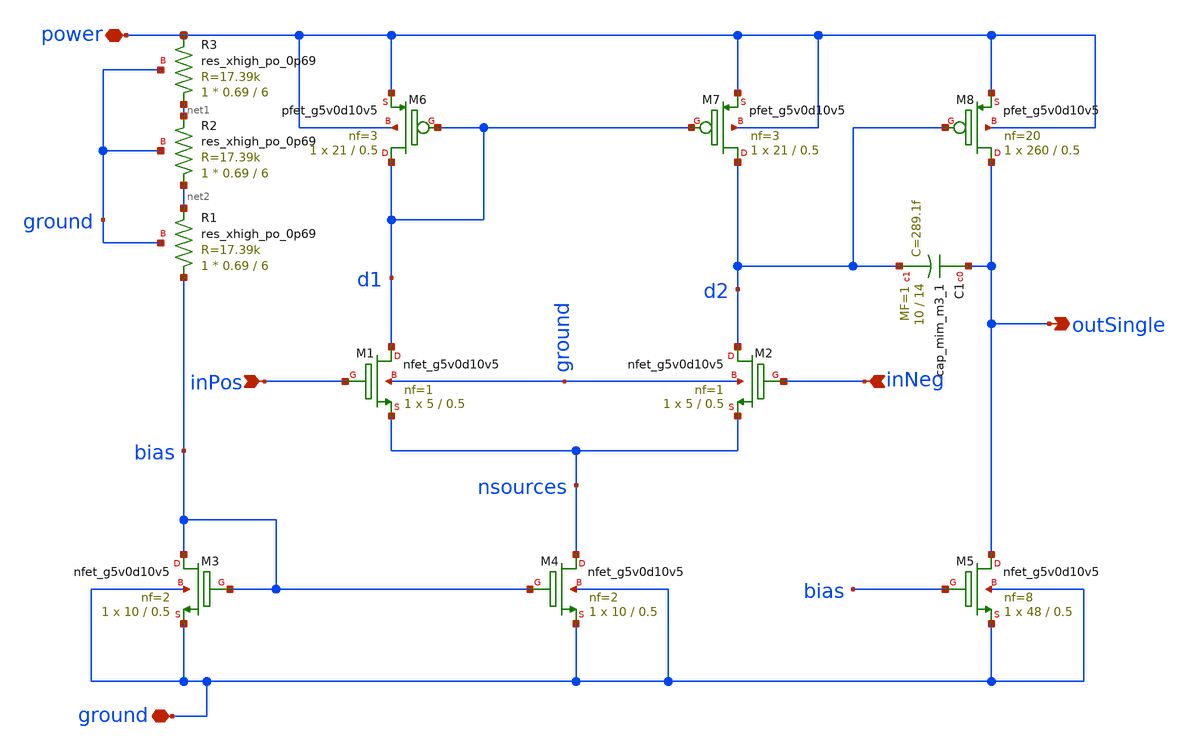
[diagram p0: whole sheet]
** sch_path: dev/opamp/miel21_opamp.sch
**.subckt miel21_opamp inPos inNeg outSingle power ground
*.ipin inPos
*.ipin inNeg
*.opin outSingle
*.iopin power
*.iopin ground
XM6 d1 d1 power power sky130_fd_pr__pfet_g5v0d10v5 L=0.5 W=21 nf=3 ad='int((nf+1)/2) * W/nf * 0.29' as='int((nf+2)/2) * W/nf * 0.29'
+ pd='2*int((nf+1)/2) * (W/nf + 0.29)' ps='2*int((nf+2)/2) * (W/nf + 0.29)' nrd='0.29 / W' nrs='0.29 / W'
+ sa=0 sb=0 sd=0 mult=1 m=1
XM7 d2 d1 power power sky130_fd_pr__pfet_g5v0d10v5 L=0.5 W=21 nf=3 ad='int((nf+1)/2) * W/nf * 0.29' as='int((nf+2)/2) * W/nf * 0.29'
+ pd='2*int((nf+1)/2) * (W/nf + 0.29)' ps='2*int((nf+2)/2) * (W/nf + 0.29)' nrd='0.29 / W' nrs='0.29 / W'
+ sa=0 sb=0 sd=0 mult=1 m=1
XM8 outSingle d2 power power sky130_fd_pr__pfet_g5v0d10v5 L=0.5 W=260 nf=20 ad='int((nf+1)/2) * W/nf * 0.29'
+ as='int((nf+2)/2) * W/nf * 0.29' pd='2*int((nf+1)/2) * (W/nf + 0.29)' ps='2*int((nf+2)/2) * (W/nf + 0.29)'
+ nrd='0.29 / W' nrs='0.29 / W' sa=0 sb=0 sd=0 mult=1 m=1
XM1 d1 inPos nsources ground sky130_fd_pr__nfet_g5v0d10v5 L=0.5 W=5 nf=1 ad='int((nf+1)/2) * W/nf * 0.29'
+ as='int((nf+2)/2) * W/nf * 0.29' pd='2*int((nf+1)/2) * (W/nf + 0.29)' ps='2*int((nf+2)/2) * (W/nf + 0.29)'
+ nrd='0.29 / W' nrs='0.29 / W' sa=0 sb=0 sd=0 mult=1 m=1
XM2 d2 inNeg nsources ground sky130_fd_pr__nfet_g5v0d10v5 L=0.5 W=5 nf=1 ad='int((nf+1)/2) * W/nf * 0.29'
+ as='int((nf+2)/2) * W/nf * 0.29' pd='2*int((nf+1)/2) * (W/nf + 0.29)' ps='2*int((nf+2)/2) * (W/nf + 0.29)'
+ nrd='0.29 / W' nrs='0.29 / W' sa=0 sb=0 sd=0 mult=1 m=1
XM3 bias bias ground ground sky130_fd_pr__nfet_g5v0d10v5 L=0.5 W=10 nf=2 ad='int((nf+1)/2) * W/nf * 0.29'
+ as='int((nf+2)/2) * W/nf * 0.29' pd='2*int((nf+1)/2) * (W/nf + 0.29)' ps='2*int((nf+2)/2) * (W/nf + 0.29)'
+ nrd='0.29 / W' nrs='0.29 / W' sa=0 sb=0 sd=0 mult=1 m=1
XM4 nsources bias ground ground sky130_fd_pr__nfet_g5v0d10v5 L=0.5 W=10 nf=2 ad='int((nf+1)/2) * W/nf * 0.29'
+ as='int((nf+2)/2) * W/nf * 0.29' pd='2*int((nf+1)/2) * (W/nf + 0.29)' ps='2*int((nf+2)/2) * (W/nf + 0.29)'
+ nrd='0.29 / W' nrs='0.29 / W' sa=0 sb=0 sd=0 mult=1 m=1
XM5 outSingle bias ground ground sky130_fd_pr__nfet_g5v0d10v5 L=0.5 W=48 nf=8 ad='int((nf+1)/2) * W/nf * 0.29'
+ as='int((nf+2)/2) * W/nf * 0.29' pd='2*int((nf+1)/2) * (W/nf + 0.29)' ps='2*int((nf+2)/2) * (W/nf + 0.29)'
+ nrd='0.29 / W' nrs='0.29 / W' sa=0 sb=0 sd=0 mult=1 m=1
XR1 bias net2 ground sky130_fd_pr__res_xhigh_po_0p69 L=6 mult=1 m=1
XC1 outSingle d2 sky130_fd_pr__cap_mim_m3_1 W=10 L=14 MF=1 m=1
XR2 net2 net1 ground sky130_fd_pr__res_xhigh_po_0p69 L=6 mult=1 m=1
XR3 net1 power ground sky130_fd_pr__res_xhigh_po_0p69 L=6 mult=1 m=1
**.ends
.end
